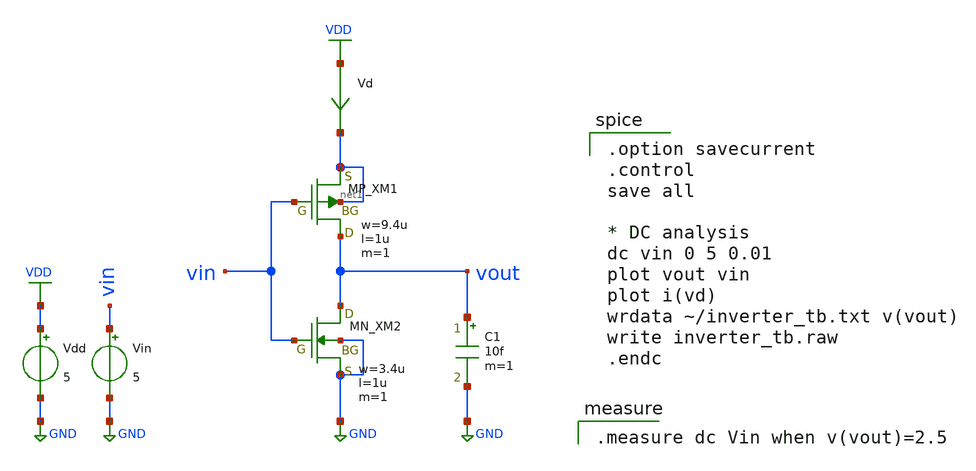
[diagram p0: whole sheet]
** sch_path: inverter/inverter_Seigo_Mitarai_tb.sch
**.subckt inverter_Seigo_Mitarai_tb
XXM1 vout vin net1 net1 PMOS w=9.4u l=1u nrd=0 nrs=0 m=1
XXM2 vout vin GND GND NMOS w=3.4u l=1u nrd=0 nrs=0 m=1
Vdd VDD GND 5
Vin vin GND 5
C1 vout GND 10f m=1
Vd VDD net1 0
.save i(vd)
**** begin user architecture code
 .include $::LIB/ip62_models

.option savecurrent
.control
save all

* DC analysis
dc vin 0 5 0.01
plot vout vin
plot i(vd)
wrdata ~/inverter_tb.txt v(vout)
write inverter_tb.raw
.endc



.measure dc Vin when v(vout)=2.5


**** end user architecture code
**.ends
.GLOBAL GND
.GLOBAL VDD
.end
